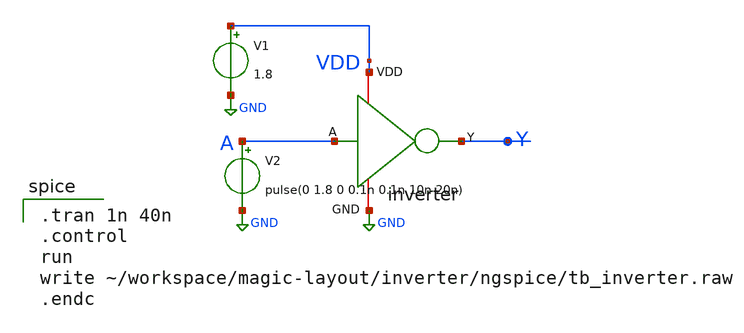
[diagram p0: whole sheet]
** sch_path: inverter/xschem/tb_inverter.sch
**.subckt tb_inverter
x1 VDD Y A GND inverter
V1 VDD GND 1.8
V2 A GND pulse(0 1.8 0 0.1n 0.1n 10n 20n)
**** begin user architecture code

.lib /foss/pdks/volare/sky130/versions/0fe599b2afb6708d281543108caf8310912f54af/sky130A/libs.tech/ngspice/sky130.lib.spice tt


.tran 1n 40n
.control
run
write ~/workspace/magic-layout/inverter/ngspice/tb_inverter.raw
.endc

**** end user architecture code
**.ends

* expanding   symbol:  inverter.sym # of pins=4
** sym_path: inverter/xschem/inverter.sym
** sch_path: inverter/xschem/inverter.sch
.subckt inverter VDD Y A GND
*.iopin GND
*.iopin VDD
*.opin Y
*.ipin A
XM1 Y A VDD VDD sky130_fd_pr__pfet_01v8 L=0.5 W=2 nf=1 ad='int((nf+1)/2) * W/nf * 0.29' as='int((nf+2)/2) * W/nf * 0.29'
+ pd='2*int((nf+1)/2) * (W/nf + 0.29)' ps='2*int((nf+2)/2) * (W/nf + 0.29)' nrd='0.29 / W' nrs='0.29 / W'
+ sa=0 sb=0 sd=0 mult=1 m=1
XM2 Y A GND GND sky130_fd_pr__nfet_01v8 L=0.15 W=1 nf=1 ad='int((nf+1)/2) * W/nf * 0.29' as='int((nf+2)/2) * W/nf * 0.29'
+ pd='2*int((nf+1)/2) * (W/nf + 0.29)' ps='2*int((nf+2)/2) * (W/nf + 0.29)' nrd='0.29 / W' nrs='0.29 / W'
+ sa=0 sb=0 sd=0 mult=1 m=1
.ends

.GLOBAL GND
.end
